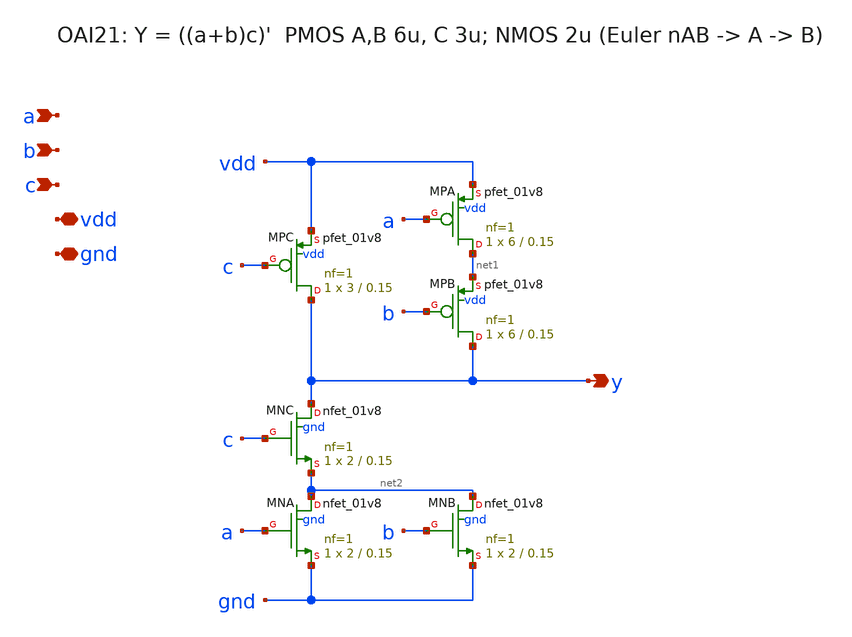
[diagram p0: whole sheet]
** sch_path: proj/xschem/oai21.sch
**.subckt oai21 a b c y vdd gnd
*.ipin a
*.ipin b
*.ipin c
*.opin y
*.iopin vdd
*.iopin gnd
XMPC y c vdd vdd sky130_fd_pr__pfet_01v8 L=0.15 W=3 nf=1 ad='int((1 + 1)/2) * 3 / 1 * 0.29' as='int((1 + 2)/2) * 3 / 1 * 0.29'
+ pd='2*int((1 + 1)/2) * (3 / 1 + 0.29)' ps='2*int((1 + 2)/2) * (3 / 1 + 0.29)' nrd='0.29 / 3 ' nrs='0.29 / 3 '
+ sa=0 sb=0 sd=0 mult=1 m=1
XMPA net1 a vdd vdd sky130_fd_pr__pfet_01v8 L=0.15 W=6 nf=1 ad='int((1 + 1)/2) * 6 / 1 * 0.29' as='int((1 + 2)/2) * 6 / 1 * 0.29'
+ pd='2*int((1 + 1)/2) * (6 / 1 + 0.29)' ps='2*int((1 + 2)/2) * (6 / 1 + 0.29)' nrd='0.29 / 6 ' nrs='0.29 / 6 '
+ sa=0 sb=0 sd=0 mult=1 m=1
XMPB y b net1 vdd sky130_fd_pr__pfet_01v8 L=0.15 W=6 nf=1 ad='int((1 + 1)/2) * 6 / 1 * 0.29' as='int((1 + 2)/2) * 6 / 1 * 0.29'
+ pd='2*int((1 + 1)/2) * (6 / 1 + 0.29)' ps='2*int((1 + 2)/2) * (6 / 1 + 0.29)' nrd='0.29 / 6 ' nrs='0.29 / 6 '
+ sa=0 sb=0 sd=0 mult=1 m=1
XMNC y c net2 gnd sky130_fd_pr__nfet_01v8 L=0.15 W=2 nf=1 ad='int((nf+1)/2) * W/nf * 0.29' as='int((nf+2)/2) * W/nf * 0.29'
+ pd='2*int((nf+1)/2) * (W/nf + 0.29)' ps='2*int((nf+2)/2) * (W/nf + 0.29)' nrd='0.29 / W' nrs='0.29 / W'
+ sa=0 sb=0 sd=0 mult=1 m=1
XMNA net2 a gnd gnd sky130_fd_pr__nfet_01v8 L=0.15 W=2 nf=1 ad='int((nf+1)/2) * W/nf * 0.29' as='int((nf+2)/2) * W/nf * 0.29'
+ pd='2*int((nf+1)/2) * (W/nf + 0.29)' ps='2*int((nf+2)/2) * (W/nf + 0.29)' nrd='0.29 / W' nrs='0.29 / W'
+ sa=0 sb=0 sd=0 mult=1 m=1
XMNB net2 b gnd gnd sky130_fd_pr__nfet_01v8 L=0.15 W=2 nf=1 ad='int((nf+1)/2) * W/nf * 0.29' as='int((nf+2)/2) * W/nf * 0.29'
+ pd='2*int((nf+1)/2) * (W/nf + 0.29)' ps='2*int((nf+2)/2) * (W/nf + 0.29)' nrd='0.29 / W' nrs='0.29 / W'
+ sa=0 sb=0 sd=0 mult=1 m=1
**.ends
.end
